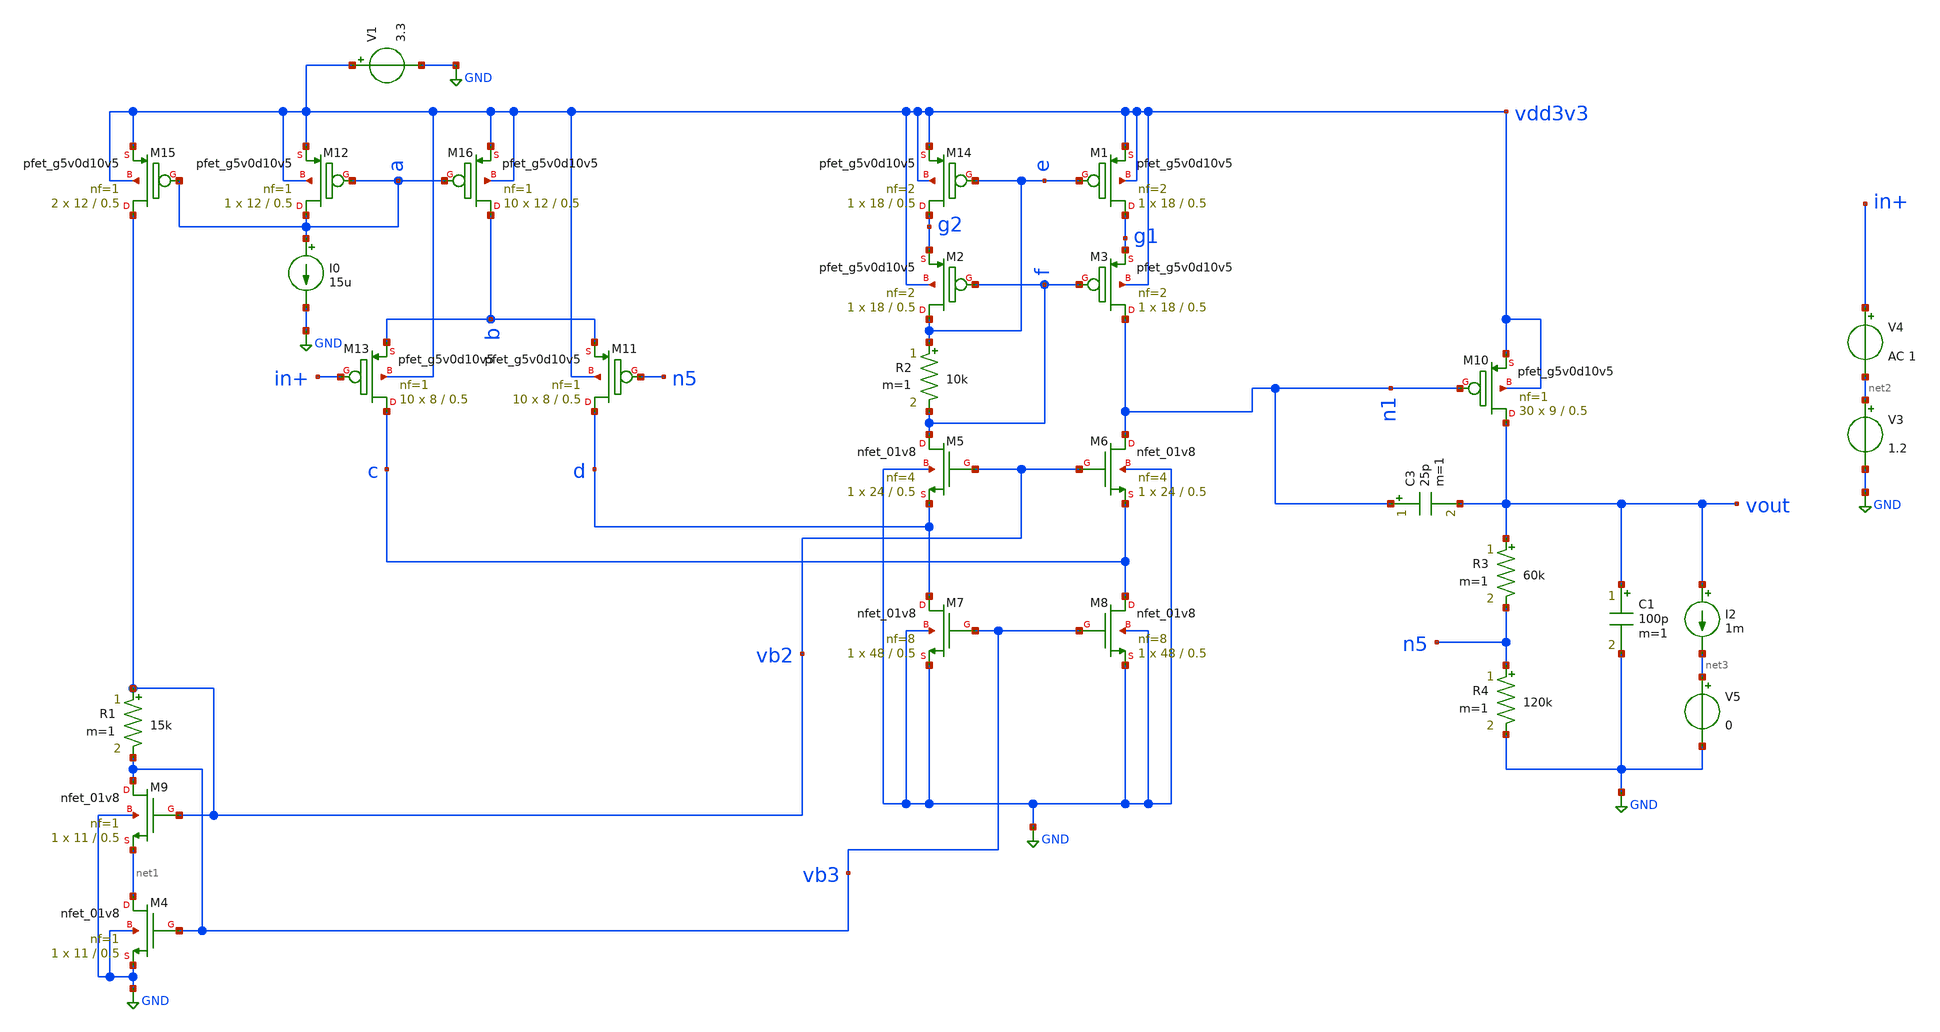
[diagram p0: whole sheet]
** sch_path: analog/analog_ldo/ceyda_src/single_ldo_tran.sch
**.subckt single_ldo_tran
R1 vb2 vb3 15k m=1
I0 a GND 15u
V1 vdd3v3 GND 3.3
R2 e f 10k m=1
XM9 vb3 vb2 net1 GND sky130_fd_pr__nfet_01v8 L=0.5 W=11 nf=1 ad='int((nf+1)/2) * W/nf * 0.29' as='int((nf+2)/2) * W/nf * 0.29'
+ pd='2*int((nf+1)/2) * (W/nf + 0.29)' ps='2*int((nf+2)/2) * (W/nf + 0.29)' nrd='0.29 / W' nrs='0.29 / W'
+ sa=0 sb=0 sd=0 mult=1 m=1
XM4 net1 vb3 GND GND sky130_fd_pr__nfet_01v8 L=0.5 W=11 nf=1 ad='int((nf+1)/2) * W/nf * 0.29' as='int((nf+2)/2) * W/nf * 0.29'
+ pd='2*int((nf+1)/2) * (W/nf + 0.29)' ps='2*int((nf+2)/2) * (W/nf + 0.29)' nrd='0.29 / W' nrs='0.29 / W'
+ sa=0 sb=0 sd=0 mult=1 m=1
XM5 f vb2 d GND sky130_fd_pr__nfet_01v8 L=0.5 W=24 nf=4 ad='int((nf+1)/2) * W/nf * 0.29' as='int((nf+2)/2) * W/nf * 0.29'
+ pd='2*int((nf+1)/2) * (W/nf + 0.29)' ps='2*int((nf+2)/2) * (W/nf + 0.29)' nrd='0.29 / W' nrs='0.29 / W'
+ sa=0 sb=0 sd=0 mult=1 m=1
XM6 n1 vb2 c GND sky130_fd_pr__nfet_01v8 L=0.5 W=24 nf=4 ad='int((nf+1)/2) * W/nf * 0.29' as='int((nf+2)/2) * W/nf * 0.29'
+ pd='2*int((nf+1)/2) * (W/nf + 0.29)' ps='2*int((nf+2)/2) * (W/nf + 0.29)' nrd='0.29 / W' nrs='0.29 / W'
+ sa=0 sb=0 sd=0 mult=1 m=1
XM7 d vb3 GND GND sky130_fd_pr__nfet_01v8 L=0.5 W=48 nf=8 ad='int((nf+1)/2) * W/nf * 0.29' as='int((nf+2)/2) * W/nf * 0.29'
+ pd='2*int((nf+1)/2) * (W/nf + 0.29)' ps='2*int((nf+2)/2) * (W/nf + 0.29)' nrd='0.29 / W' nrs='0.29 / W'
+ sa=0 sb=0 sd=0 mult=1 m=1
XM8 c vb3 GND GND sky130_fd_pr__nfet_01v8 L=0.5 W=48 nf=8 ad='int((nf+1)/2) * W/nf * 0.29' as='int((nf+2)/2) * W/nf * 0.29'
+ pd='2*int((nf+1)/2) * (W/nf + 0.29)' ps='2*int((nf+2)/2) * (W/nf + 0.29)' nrd='0.29 / W' nrs='0.29 / W'
+ sa=0 sb=0 sd=0 mult=1 m=1
XM15 vb2 a vdd3v3 vdd3v3 sky130_fd_pr__pfet_g5v0d10v5 L=0.5 W=12 nf=1 ad='int((nf+1)/2) * W/nf * 0.29'
+ as='int((nf+2)/2) * W/nf * 0.29' pd='2*int((nf+1)/2) * (W/nf + 0.29)' ps='2*int((nf+2)/2) * (W/nf + 0.29)'
+ nrd='0.29 / W' nrs='0.29 / W' sa=0 sb=0 sd=0 mult=2 m=2
XM12 a a vdd3v3 vdd3v3 sky130_fd_pr__pfet_g5v0d10v5 L=0.5 W=12 nf=1 ad='int((nf+1)/2) * W/nf * 0.29'
+ as='int((nf+2)/2) * W/nf * 0.29' pd='2*int((nf+1)/2) * (W/nf + 0.29)' ps='2*int((nf+2)/2) * (W/nf + 0.29)'
+ nrd='0.29 / W' nrs='0.29 / W' sa=0 sb=0 sd=0 mult=1 m=1
XM16 b a vdd3v3 vdd3v3 sky130_fd_pr__pfet_g5v0d10v5 L=0.5 W=12 nf=1 ad='int((nf+1)/2) * W/nf * 0.29'
+ as='int((nf+2)/2) * W/nf * 0.29' pd='2*int((nf+1)/2) * (W/nf + 0.29)' ps='2*int((nf+2)/2) * (W/nf + 0.29)'
+ nrd='0.29 / W' nrs='0.29 / W' sa=0 sb=0 sd=0 mult=10 m=10
XM13 c in+ b vdd3v3 sky130_fd_pr__pfet_g5v0d10v5 L=0.5 W=8 nf=1 ad='int((nf+1)/2) * W/nf * 0.29' as='int((nf+2)/2) * W/nf * 0.29'
+ pd='2*int((nf+1)/2) * (W/nf + 0.29)' ps='2*int((nf+2)/2) * (W/nf + 0.29)' nrd='0.29 / W' nrs='0.29 / W'
+ sa=0 sb=0 sd=0 mult=10 m=10
XM11 d n5 b vdd3v3 sky130_fd_pr__pfet_g5v0d10v5 L=0.5 W=8 nf=1 ad='int((nf+1)/2) * W/nf * 0.29' as='int((nf+2)/2) * W/nf * 0.29'
+ pd='2*int((nf+1)/2) * (W/nf + 0.29)' ps='2*int((nf+2)/2) * (W/nf + 0.29)' nrd='0.29 / W' nrs='0.29 / W'
+ sa=0 sb=0 sd=0 mult=10 m=10
XM14 g2 e vdd3v3 vdd3v3 sky130_fd_pr__pfet_g5v0d10v5 L=0.5 W=18 nf=2 ad='int((nf+1)/2) * W/nf * 0.29'
+ as='int((nf+2)/2) * W/nf * 0.29' pd='2*int((nf+1)/2) * (W/nf + 0.29)' ps='2*int((nf+2)/2) * (W/nf + 0.29)'
+ nrd='0.29 / W' nrs='0.29 / W' sa=0 sb=0 sd=0 mult=1 m=1
XM2 e f g2 vdd3v3 sky130_fd_pr__pfet_g5v0d10v5 L=0.5 W=18 nf=2 ad='int((nf+1)/2) * W/nf * 0.29' as='int((nf+2)/2) * W/nf * 0.29'
+ pd='2*int((nf+1)/2) * (W/nf + 0.29)' ps='2*int((nf+2)/2) * (W/nf + 0.29)' nrd='0.29 / W' nrs='0.29 / W'
+ sa=0 sb=0 sd=0 mult=1 m=1
XM1 g1 e vdd3v3 vdd3v3 sky130_fd_pr__pfet_g5v0d10v5 L=0.5 W=18 nf=2 ad='int((nf+1)/2) * W/nf * 0.29'
+ as='int((nf+2)/2) * W/nf * 0.29' pd='2*int((nf+1)/2) * (W/nf + 0.29)' ps='2*int((nf+2)/2) * (W/nf + 0.29)'
+ nrd='0.29 / W' nrs='0.29 / W' sa=0 sb=0 sd=0 mult=1 m=1
XM3 n1 f g1 vdd3v3 sky130_fd_pr__pfet_g5v0d10v5 L=0.5 W=18 nf=2 ad='int((nf+1)/2) * W/nf * 0.29' as='int((nf+2)/2) * W/nf * 0.29'
+ pd='2*int((nf+1)/2) * (W/nf + 0.29)' ps='2*int((nf+2)/2) * (W/nf + 0.29)' nrd='0.29 / W' nrs='0.29 / W'
+ sa=0 sb=0 sd=0 mult=1 m=1
C1 vout GND 100p m=1
R3 vout n5 60k m=1
R4 n5 GND 120k m=1
XM10 vout n1 vdd3v3 vdd3v3 sky130_fd_pr__pfet_g5v0d10v5 L=0.5 W=9 nf=1 ad='int((nf+1)/2) * W/nf * 0.29'
+ as='int((nf+2)/2) * W/nf * 0.29' pd='2*int((nf+1)/2) * (W/nf + 0.29)' ps='2*int((nf+2)/2) * (W/nf + 0.29)'
+ nrd='0.29 / W' nrs='0.29 / W' sa=0 sb=0 sd=0 mult=30 m=30
V3 net2 GND 1.2
V4 in+ net2 AC 1
C3 n1 vout 25p m=1
V5 net3 GND 0
I2 vout net3 1m
**** begin user architecture code

** opencircuitdesign pdks install
.lib $::SKYWATER_MODELS/sky130.lib.spice tt





.param R_i = 5k
.option method=Gear
*.ic v(vout)=1.8 v(n5)=1.2
.control
set color0=white
set units= degrees
*set sqrnoise
save all


tran .1u 20u
*let gmdp= @m.xm14.msky130_fd_pr__pfet_01v8[gm]
plot vb2 vb3
plot vout
plot n1
plot a b c d e f

*reset
*ac dec 100 1 1G
*plot vdb(vout)
*plot phase(vout)
*plot vdb(outn)
*plot inp inn out1

*meas ac gbw when vdb(vout)=0
*meas ac gbw_2 when vout=1

*reset
*noise v(vout) V4 dec 100 1 52Meg
*print inoise_total onoise_total
*setplot noise1
*plot inoise_spectrum xlog ylog
*plot onoise_spectrum xlog ylog


show all
.endc


**** end user architecture code
**.ends
.GLOBAL GND
.end
